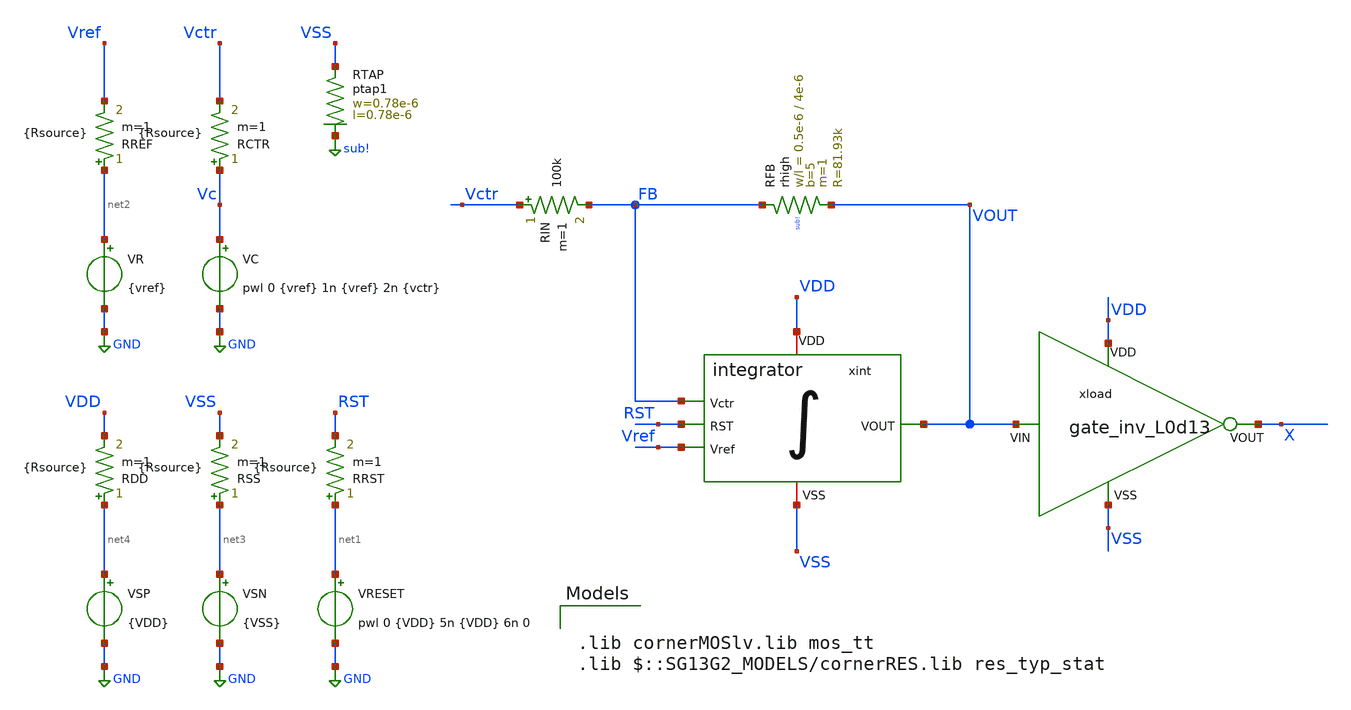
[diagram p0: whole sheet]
** sch_path: work/integrator/xschem/integrator_closedloop.sch
**.subckt integrator_closedloop
xint Vref VSS VDD RST FB VOUT integrator
xload VDD VOUT X VSS gate_inv_L0d13
VRESET net1 GND pwl 0 {VDD} 5n {VDD} 6n 0
VSN net3 GND {VSS}
VR net2 GND {vref}
VC Vc GND pwl 0 {vref} 1n {vref} 2n {vctr}
RDD net4 VDD {Rsource} m=1
RSS net3 VSS {Rsource} m=1
RRST net1 RST {Rsource} m=1
RREF net2 Vref {Rsource} m=1
RCTR Vc Vctr {Rsource} m=1
VSP net4 GND {VDD}
XRTAP VSS sub! ptap1 R=262.8 w=0.78e-6 l=0.78e-6
XRFB FB VOUT sub! rhigh w=0.5e-6 l=4e-6 m=1 b=5 mm_ok=1
RIN Vctr FB 100k m=1
**** begin user architecture code



.param Vctr = 1.2
.param Vref = 0.6
.param VDD = 1.2
.param VSS = 0
.param Rsource = 10

.save all

.control

* >> Variables <<
let Vhigh = 1.2
let Vmid = Vhigh * 0.5
let tstop = 25n
let tstep = tstop/10k

* Run transient analysis
tran $&tstep $&tstop

meas TRAN T_ctr TRIG v(xint.p1) VAL=Vmid rise=2 TARG v(xint.p1) VAL=Vmid rise=3
let F_ctr = 1 / T_ctr
meas TRAN T_ref TRIG v(xint.r1) VAL=Vmid rise=2 TARG v(xint.r1) VAL=Vmid rise=3
let F_ref = 1 / T_ref

print F_ctr/1e+06 F_ref/1e+06

meas tran i_INT AVG i(VSP) from=6n to=$&tstop
let i_INT_AVG=-1*i_INT

print i_INT_AVG

plot Vctr RST
plot FB Vref
plot Vout
plot xint.p1 xint.r1

.endc



.lib cornerMOSlv.lib mos_tt
.lib $::SG13G2_MODELS/cornerRES.lib res_typ_stat

**** end user architecture code
**.ends
.GLOBAL GND
.GLOBAL sub!
.end
